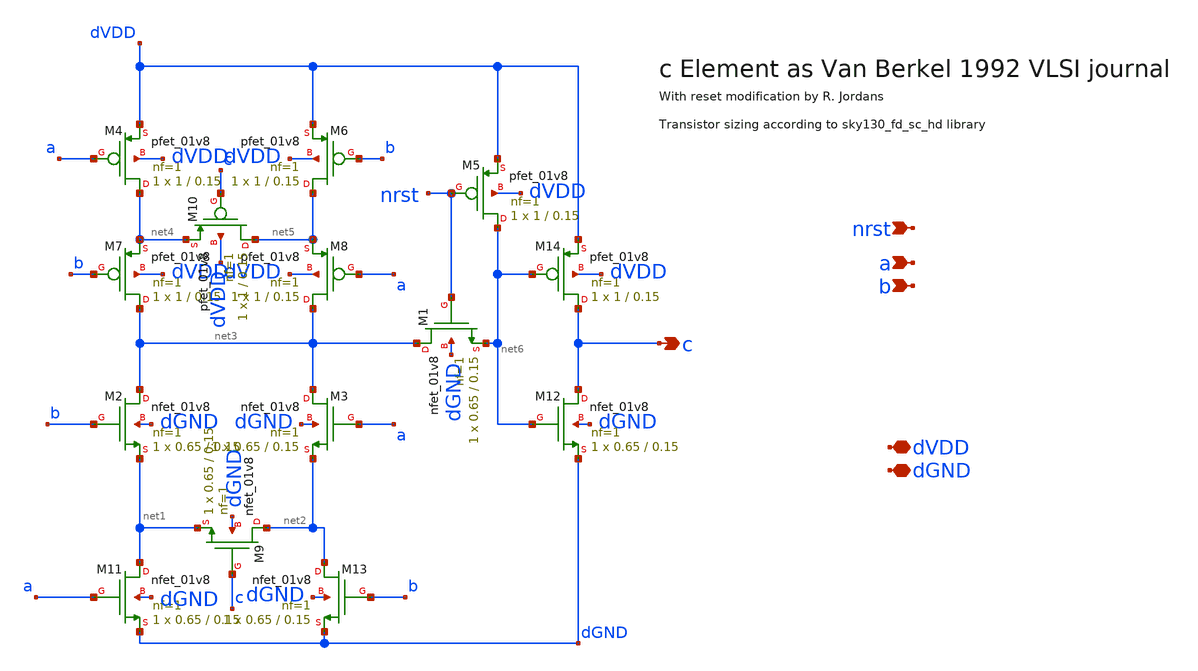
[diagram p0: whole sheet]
** sch_path: design/xschem/c_element_rj.sch
**.subckt c_element_rj dGND dVDD c b a nrst
*.iopin dGND
*.iopin dVDD
*.opin c
*.ipin b
*.ipin a
*.ipin nrst
XM14 c net6 dVDD dVDD sky130_fd_pr__pfet_01v8 L=0.15 W=1 nf=1 ad='int((nf+1)/2) * W/nf * 0.29' as='int((nf+2)/2) * W/nf * 0.29'
+ pd='2*int((nf+1)/2) * (W/nf + 0.29)' ps='2*int((nf+2)/2) * (W/nf + 0.29)' nrd='0.29 / W' nrs='0.29 / W'
+ sa=0 sb=0 sd=0 mult=1 m=1
XM5 net6 nrst dVDD dVDD sky130_fd_pr__pfet_01v8 L=0.15 W=1 nf=1 ad='int((nf+1)/2) * W/nf * 0.29' as='int((nf+2)/2) * W/nf * 0.29'
+ pd='2*int((nf+1)/2) * (W/nf + 0.29)' ps='2*int((nf+2)/2) * (W/nf + 0.29)' nrd='0.29 / W' nrs='0.29 / W'
+ sa=0 sb=0 sd=0 mult=1 m=1
XM6 net5 b dVDD dVDD sky130_fd_pr__pfet_01v8 L=0.15 W=1 nf=1 ad='int((nf+1)/2) * W/nf * 0.29' as='int((nf+2)/2) * W/nf * 0.29'
+ pd='2*int((nf+1)/2) * (W/nf + 0.29)' ps='2*int((nf+2)/2) * (W/nf + 0.29)' nrd='0.29 / W' nrs='0.29 / W'
+ sa=0 sb=0 sd=0 mult=1 m=1
XM4 net4 a dVDD dVDD sky130_fd_pr__pfet_01v8 L=0.15 W=1 nf=1 ad='int((nf+1)/2) * W/nf * 0.29' as='int((nf+2)/2) * W/nf * 0.29'
+ pd='2*int((nf+1)/2) * (W/nf + 0.29)' ps='2*int((nf+2)/2) * (W/nf + 0.29)' nrd='0.29 / W' nrs='0.29 / W'
+ sa=0 sb=0 sd=0 mult=1 m=1
XM7 net3 b net4 dVDD sky130_fd_pr__pfet_01v8 L=0.15 W=1 nf=1 ad='int((nf+1)/2) * W/nf * 0.29' as='int((nf+2)/2) * W/nf * 0.29'
+ pd='2*int((nf+1)/2) * (W/nf + 0.29)' ps='2*int((nf+2)/2) * (W/nf + 0.29)' nrd='0.29 / W' nrs='0.29 / W'
+ sa=0 sb=0 sd=0 mult=1 m=1
XM8 net3 a net5 dVDD sky130_fd_pr__pfet_01v8 L=0.15 W=1 nf=1 ad='int((nf+1)/2) * W/nf * 0.29' as='int((nf+2)/2) * W/nf * 0.29'
+ pd='2*int((nf+1)/2) * (W/nf + 0.29)' ps='2*int((nf+2)/2) * (W/nf + 0.29)' nrd='0.29 / W' nrs='0.29 / W'
+ sa=0 sb=0 sd=0 mult=1 m=1
XM10 net5 c net4 dVDD sky130_fd_pr__pfet_01v8 L=0.15 W=1 nf=1 ad='int((nf+1)/2) * W/nf * 0.29' as='int((nf+2)/2) * W/nf * 0.29'
+ pd='2*int((nf+1)/2) * (W/nf + 0.29)' ps='2*int((nf+2)/2) * (W/nf + 0.29)' nrd='0.29 / W' nrs='0.29 / W'
+ sa=0 sb=0 sd=0 mult=1 m=1
XM12 c net6 dGND dGND sky130_fd_pr__nfet_01v8 L=0.15 W=0.65 nf=1 ad='int((nf+1)/2) * W/nf * 0.29' as='int((nf+2)/2) * W/nf * 0.29'
+ pd='2*int((nf+1)/2) * (W/nf + 0.29)' ps='2*int((nf+2)/2) * (W/nf + 0.29)' nrd='0.29 / W' nrs='0.29 / W'
+ sa=0 sb=0 sd=0 mult=1 m=1
XM1 net3 nrst net6 dGND sky130_fd_pr__nfet_01v8 L=0.15 W=0.65 nf=1 ad='int((nf+1)/2) * W/nf * 0.29' as='int((nf+2)/2) * W/nf * 0.29'
+ pd='2*int((nf+1)/2) * (W/nf + 0.29)' ps='2*int((nf+2)/2) * (W/nf + 0.29)' nrd='0.29 / W' nrs='0.29 / W'
+ sa=0 sb=0 sd=0 mult=1 m=1
XM2 net3 b net1 dGND sky130_fd_pr__nfet_01v8 L=0.15 W=0.65 nf=1 ad='int((nf+1)/2) * W/nf * 0.29' as='int((nf+2)/2) * W/nf * 0.29'
+ pd='2*int((nf+1)/2) * (W/nf + 0.29)' ps='2*int((nf+2)/2) * (W/nf + 0.29)' nrd='0.29 / W' nrs='0.29 / W'
+ sa=0 sb=0 sd=0 mult=1 m=1
XM3 net3 a net2 dGND sky130_fd_pr__nfet_01v8 L=0.15 W=0.65 nf=1 ad='int((nf+1)/2) * W/nf * 0.29' as='int((nf+2)/2) * W/nf * 0.29'
+ pd='2*int((nf+1)/2) * (W/nf + 0.29)' ps='2*int((nf+2)/2) * (W/nf + 0.29)' nrd='0.29 / W' nrs='0.29 / W'
+ sa=0 sb=0 sd=0 mult=1 m=1
XM9 net2 c net1 dGND sky130_fd_pr__nfet_01v8 L=0.15 W=0.65 nf=1 ad='int((nf+1)/2) * W/nf * 0.29' as='int((nf+2)/2) * W/nf * 0.29'
+ pd='2*int((nf+1)/2) * (W/nf + 0.29)' ps='2*int((nf+2)/2) * (W/nf + 0.29)' nrd='0.29 / W' nrs='0.29 / W'
+ sa=0 sb=0 sd=0 mult=1 m=1
XM11 net1 a dGND dGND sky130_fd_pr__nfet_01v8 L=0.15 W=0.65 nf=1 ad='int((nf+1)/2) * W/nf * 0.29' as='int((nf+2)/2) * W/nf * 0.29'
+ pd='2*int((nf+1)/2) * (W/nf + 0.29)' ps='2*int((nf+2)/2) * (W/nf + 0.29)' nrd='0.29 / W' nrs='0.29 / W'
+ sa=0 sb=0 sd=0 mult=1 m=1
XM13 net2 b dGND dGND sky130_fd_pr__nfet_01v8 L=0.15 W=0.65 nf=1 ad='int((nf+1)/2) * W/nf * 0.29' as='int((nf+2)/2) * W/nf * 0.29'
+ pd='2*int((nf+1)/2) * (W/nf + 0.29)' ps='2*int((nf+2)/2) * (W/nf + 0.29)' nrd='0.29 / W' nrs='0.29 / W'
+ sa=0 sb=0 sd=0 mult=1 m=1
**.ends
.end
